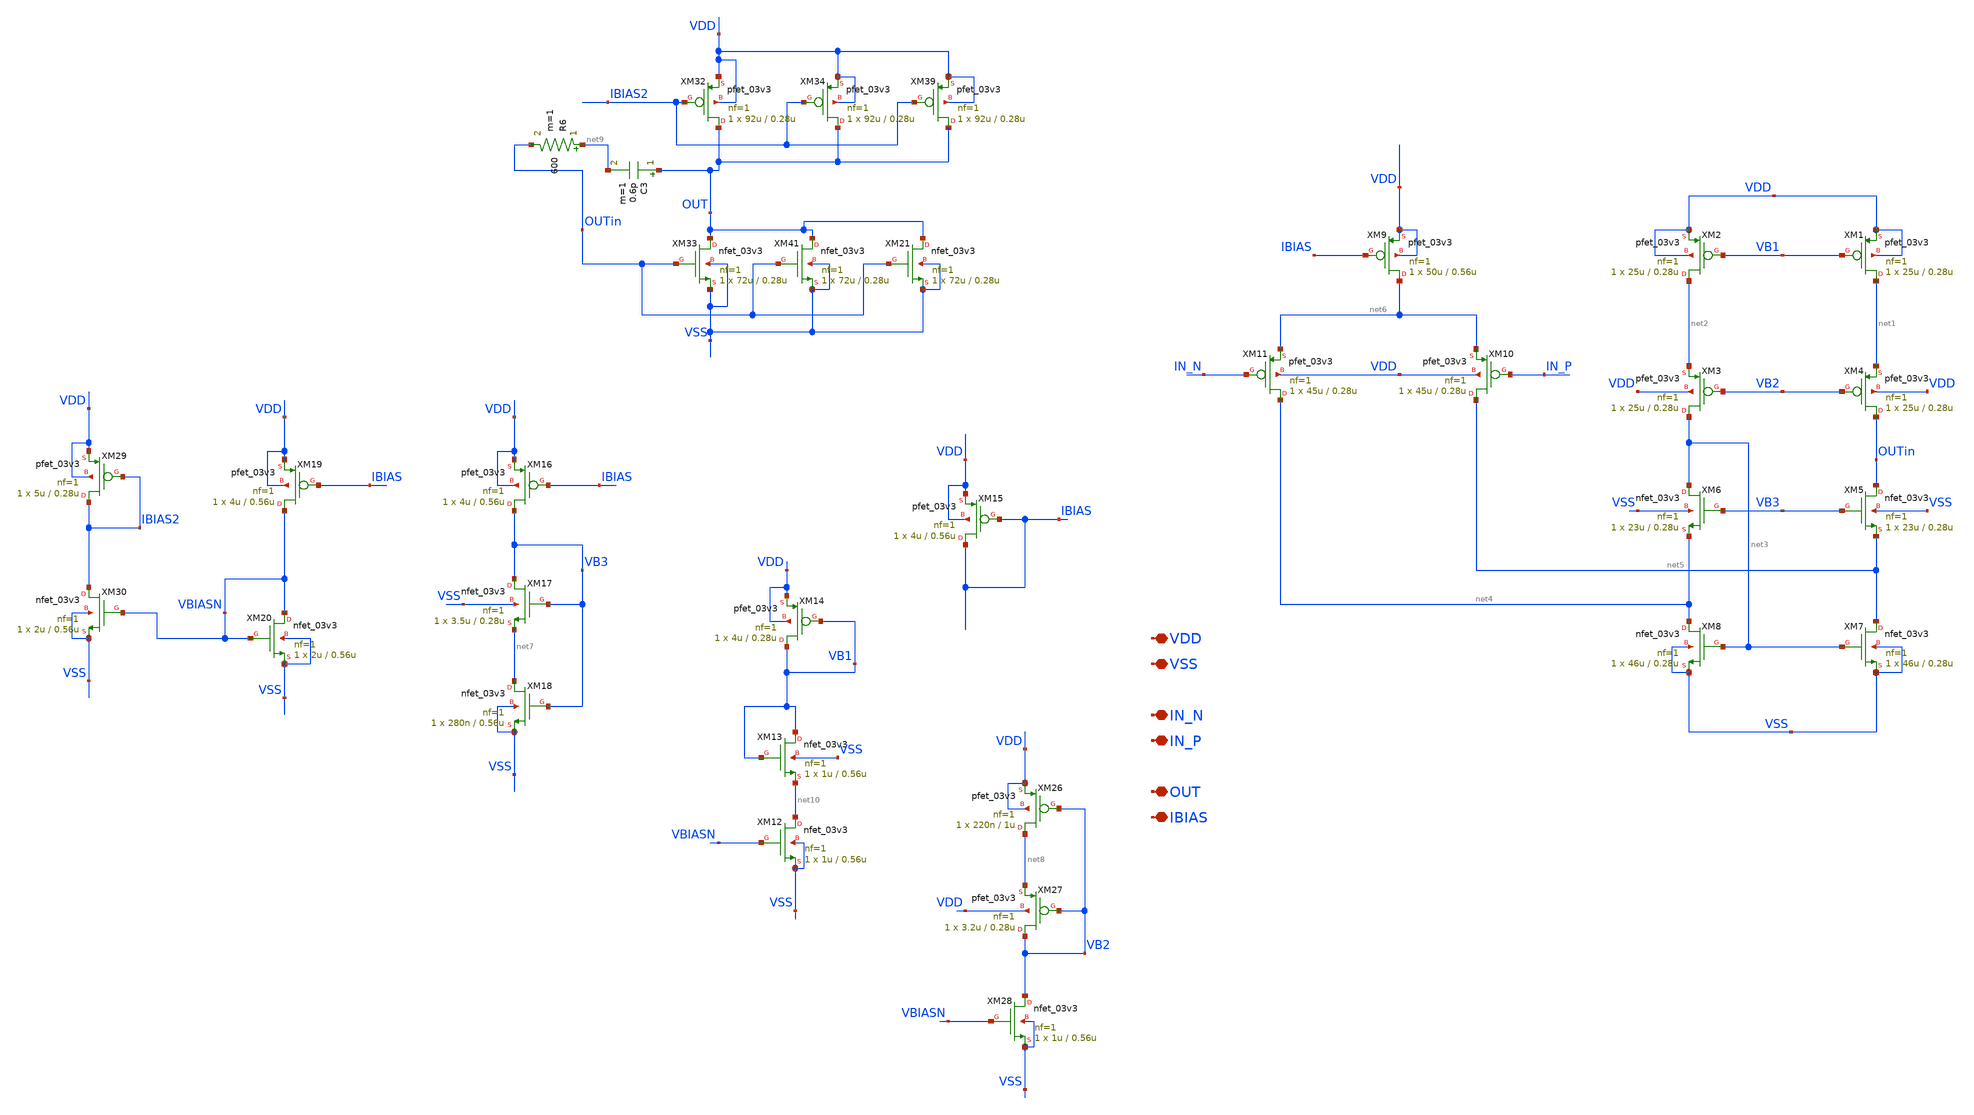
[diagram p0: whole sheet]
** sch_path: SCOP_INPUT_AND_MUX_PAKISTAN_03/Xschem/Folded_Cascode_Amplifier/Folded_opamp_single.sch
**.subckt Folded_opamp_single VDD VSS IN_N IN_P OUT IBIAS
*.iopin VDD
*.iopin VSS
*.iopin IN_N
*.iopin IN_P
*.iopin OUT
*.iopin IBIAS
XM1 net1 VB1 VDD VDD pfet_03v3 L=0.28u W=25u nf=1 ad='int((nf+1)/2) * W/nf * 0.18u' as='int((nf+2)/2) * W/nf * 0.18u'
+ pd='2*int((nf+1)/2) * (W/nf + 0.18u)' ps='2*int((nf+2)/2) * (W/nf + 0.18u)' nrd='0.18u / W' nrs='0.18u / W'
+ sa=0 sb=0 sd=0 m=1
XM2 net2 VB1 VDD VDD pfet_03v3 L=0.28u W=25u nf=1 ad='int((nf+1)/2) * W/nf * 0.18u' as='int((nf+2)/2) * W/nf * 0.18u'
+ pd='2*int((nf+1)/2) * (W/nf + 0.18u)' ps='2*int((nf+2)/2) * (W/nf + 0.18u)' nrd='0.18u / W' nrs='0.18u / W'
+ sa=0 sb=0 sd=0 m=1
XM3 net3 VB2 net2 VDD pfet_03v3 L=0.28u W=25u nf=1 ad='int((nf+1)/2) * W/nf * 0.18u' as='int((nf+2)/2) * W/nf * 0.18u'
+ pd='2*int((nf+1)/2) * (W/nf + 0.18u)' ps='2*int((nf+2)/2) * (W/nf + 0.18u)' nrd='0.18u / W' nrs='0.18u / W'
+ sa=0 sb=0 sd=0 m=1
XM4 OUTin VB2 net1 VDD pfet_03v3 L=0.28u W=25u nf=1 ad='int((nf+1)/2) * W/nf * 0.18u' as='int((nf+2)/2) * W/nf * 0.18u'
+ pd='2*int((nf+1)/2) * (W/nf + 0.18u)' ps='2*int((nf+2)/2) * (W/nf + 0.18u)' nrd='0.18u / W' nrs='0.18u / W'
+ sa=0 sb=0 sd=0 m=1
XM5 OUTin VB3 net5 VSS nfet_03v3 L=0.28u W=23u nf=1 ad='int((nf+1)/2) * W/nf * 0.18u' as='int((nf+2)/2) * W/nf * 0.18u'
+ pd='2*int((nf+1)/2) * (W/nf + 0.18u)' ps='2*int((nf+2)/2) * (W/nf + 0.18u)' nrd='0.18u / W' nrs='0.18u / W'
+ sa=0 sb=0 sd=0 m=1
XM6 net3 VB3 net4 VSS nfet_03v3 L=0.28u W=23u nf=1 ad='int((nf+1)/2) * W/nf * 0.18u' as='int((nf+2)/2) * W/nf * 0.18u'
+ pd='2*int((nf+1)/2) * (W/nf + 0.18u)' ps='2*int((nf+2)/2) * (W/nf + 0.18u)' nrd='0.18u / W' nrs='0.18u / W'
+ sa=0 sb=0 sd=0 m=1
XM7 net5 net3 VSS VSS nfet_03v3 L=0.28u W=46u nf=1 ad='int((nf+1)/2) * W/nf * 0.18u' as='int((nf+2)/2) * W/nf * 0.18u'
+ pd='2*int((nf+1)/2) * (W/nf + 0.18u)' ps='2*int((nf+2)/2) * (W/nf + 0.18u)' nrd='0.18u / W' nrs='0.18u / W'
+ sa=0 sb=0 sd=0 m=1
XM8 net4 net3 VSS VSS nfet_03v3 L=0.28u W=46u nf=1 ad='int((nf+1)/2) * W/nf * 0.18u' as='int((nf+2)/2) * W/nf * 0.18u'
+ pd='2*int((nf+1)/2) * (W/nf + 0.18u)' ps='2*int((nf+2)/2) * (W/nf + 0.18u)' nrd='0.18u / W' nrs='0.18u / W'
+ sa=0 sb=0 sd=0 m=1
XM9 net6 IBIAS VDD VDD pfet_03v3 L=0.56u W=50u nf=1 ad='int((nf+1)/2) * W/nf * 0.18u' as='int((nf+2)/2) * W/nf * 0.18u'
+ pd='2*int((nf+1)/2) * (W/nf + 0.18u)' ps='2*int((nf+2)/2) * (W/nf + 0.18u)' nrd='0.18u / W' nrs='0.18u / W'
+ sa=0 sb=0 sd=0 m=1
XM10 net5 IN_P net6 VDD pfet_03v3 L=0.28u W=45u nf=1 ad='int((nf+1)/2) * W/nf * 0.18u' as='int((nf+2)/2) * W/nf * 0.18u'
+ pd='2*int((nf+1)/2) * (W/nf + 0.18u)' ps='2*int((nf+2)/2) * (W/nf + 0.18u)' nrd='0.18u / W' nrs='0.18u / W'
+ sa=0 sb=0 sd=0 m=1
XM11 net4 IN_N net6 VDD pfet_03v3 L=0.28u W=45u nf=1 ad='int((nf+1)/2) * W/nf * 0.18u' as='int((nf+2)/2) * W/nf * 0.18u'
+ pd='2*int((nf+1)/2) * (W/nf + 0.18u)' ps='2*int((nf+2)/2) * (W/nf + 0.18u)' nrd='0.18u / W' nrs='0.18u / W'
+ sa=0 sb=0 sd=0 m=1
XM15 IBIAS IBIAS VDD VDD pfet_03v3 L=0.56u W=4u nf=1 ad='int((nf+1)/2) * W/nf * 0.18u' as='int((nf+2)/2) * W/nf * 0.18u'
+ pd='2*int((nf+1)/2) * (W/nf + 0.18u)' ps='2*int((nf+2)/2) * (W/nf + 0.18u)' nrd='0.18u / W' nrs='0.18u / W'
+ sa=0 sb=0 sd=0 m=1
XM16 VB3 IBIAS VDD VDD pfet_03v3 L=0.56u W=4u nf=1 ad='int((nf+1)/2) * W/nf * 0.18u' as='int((nf+2)/2) * W/nf * 0.18u'
+ pd='2*int((nf+1)/2) * (W/nf + 0.18u)' ps='2*int((nf+2)/2) * (W/nf + 0.18u)' nrd='0.18u / W' nrs='0.18u / W'
+ sa=0 sb=0 sd=0 m=1
XM17 VB3 VB3 net7 VSS nfet_03v3 L=0.28u W=3.5u nf=1 ad='int((nf+1)/2) * W/nf * 0.18u' as='int((nf+2)/2) * W/nf * 0.18u'
+ pd='2*int((nf+1)/2) * (W/nf + 0.18u)' ps='2*int((nf+2)/2) * (W/nf + 0.18u)' nrd='0.18u / W' nrs='0.18u / W'
+ sa=0 sb=0 sd=0 m=1
XM18 net7 VB3 VSS VSS nfet_03v3 L=0.56u W=280n nf=1 ad='int((nf+1)/2) * W/nf * 0.18u' as='int((nf+2)/2) * W/nf * 0.18u'
+ pd='2*int((nf+1)/2) * (W/nf + 0.18u)' ps='2*int((nf+2)/2) * (W/nf + 0.18u)' nrd='0.18u / W' nrs='0.18u / W'
+ sa=0 sb=0 sd=0 m=1
XM19 VBIASN IBIAS VDD VDD pfet_03v3 L=0.56u W=4u nf=1 ad='int((nf+1)/2) * W/nf * 0.18u' as='int((nf+2)/2) * W/nf * 0.18u'
+ pd='2*int((nf+1)/2) * (W/nf + 0.18u)' ps='2*int((nf+2)/2) * (W/nf + 0.18u)' nrd='0.18u / W' nrs='0.18u / W'
+ sa=0 sb=0 sd=0 m=1
XM20 VBIASN VBIASN VSS VSS nfet_03v3 L=0.56u W=2u nf=1 ad='int((nf+1)/2) * W/nf * 0.18u' as='int((nf+2)/2) * W/nf * 0.18u'
+ pd='2*int((nf+1)/2) * (W/nf + 0.18u)' ps='2*int((nf+2)/2) * (W/nf + 0.18u)' nrd='0.18u / W' nrs='0.18u / W'
+ sa=0 sb=0 sd=0 m=1
XM26 net8 VB2 VDD VDD pfet_03v3 L=1u W=220n nf=1 ad='int((nf+1)/2) * W/nf * 0.18u' as='int((nf+2)/2) * W/nf * 0.18u'
+ pd='2*int((nf+1)/2) * (W/nf + 0.18u)' ps='2*int((nf+2)/2) * (W/nf + 0.18u)' nrd='0.18u / W' nrs='0.18u / W'
+ sa=0 sb=0 sd=0 m=1
XM27 VB2 VB2 net8 VDD pfet_03v3 L=0.28u W=3.2u nf=1 ad='int((nf+1)/2) * W/nf * 0.18u' as='int((nf+2)/2) * W/nf * 0.18u'
+ pd='2*int((nf+1)/2) * (W/nf + 0.18u)' ps='2*int((nf+2)/2) * (W/nf + 0.18u)' nrd='0.18u / W' nrs='0.18u / W'
+ sa=0 sb=0 sd=0 m=1
XM28 VB2 VBIASN VSS VSS nfet_03v3 L=0.56u W=1u nf=1 ad='int((nf+1)/2) * W/nf * 0.18u' as='int((nf+2)/2) * W/nf * 0.18u'
+ pd='2*int((nf+1)/2) * (W/nf + 0.18u)' ps='2*int((nf+2)/2) * (W/nf + 0.18u)' nrd='0.18u / W' nrs='0.18u / W'
+ sa=0 sb=0 sd=0 m=1
XM29 IBIAS2 IBIAS2 VDD VDD pfet_03v3 L=0.28u W=5u nf=1 ad='int((nf+1)/2) * W/nf * 0.18u' as='int((nf+2)/2) * W/nf * 0.18u'
+ pd='2*int((nf+1)/2) * (W/nf + 0.18u)' ps='2*int((nf+2)/2) * (W/nf + 0.18u)' nrd='0.18u / W' nrs='0.18u / W'
+ sa=0 sb=0 sd=0 m=1
XM30 IBIAS2 VBIASN VSS VSS nfet_03v3 L=0.56u W=2u nf=1 ad='int((nf+1)/2) * W/nf * 0.18u' as='int((nf+2)/2) * W/nf * 0.18u'
+ pd='2*int((nf+1)/2) * (W/nf + 0.18u)' ps='2*int((nf+2)/2) * (W/nf + 0.18u)' nrd='0.18u / W' nrs='0.18u / W'
+ sa=0 sb=0 sd=0 m=1
XM32 OUT IBIAS2 VDD VDD pfet_03v3 L=0.28u W=92u nf=1 ad='int((nf+1)/2) * W/nf * 0.18u' as='int((nf+2)/2) * W/nf * 0.18u'
+ pd='2*int((nf+1)/2) * (W/nf + 0.18u)' ps='2*int((nf+2)/2) * (W/nf + 0.18u)' nrd='0.18u / W' nrs='0.18u / W'
+ sa=0 sb=0 sd=0 m=1
XM33 OUT OUTin VSS VSS nfet_03v3 L=0.28u W=72u nf=1 ad='int((nf+1)/2) * W/nf * 0.18u' as='int((nf+2)/2) * W/nf * 0.18u'
+ pd='2*int((nf+1)/2) * (W/nf + 0.18u)' ps='2*int((nf+2)/2) * (W/nf + 0.18u)' nrd='0.18u / W' nrs='0.18u / W'
+ sa=0 sb=0 sd=0 m=1
C3 OUT net9 0.6p m=1
XM34 OUT IBIAS2 VDD VDD pfet_03v3 L=0.28u W=92u nf=1 ad='int((nf+1)/2) * W/nf * 0.18u' as='int((nf+2)/2) * W/nf * 0.18u'
+ pd='2*int((nf+1)/2) * (W/nf + 0.18u)' ps='2*int((nf+2)/2) * (W/nf + 0.18u)' nrd='0.18u / W' nrs='0.18u / W'
+ sa=0 sb=0 sd=0 m=1
R6 net9 OUTin 600 m=1
XM41 OUT OUTin VSS VSS nfet_03v3 L=0.28u W=72u nf=1 ad='int((nf+1)/2) * W/nf * 0.18u' as='int((nf+2)/2) * W/nf * 0.18u'
+ pd='2*int((nf+1)/2) * (W/nf + 0.18u)' ps='2*int((nf+2)/2) * (W/nf + 0.18u)' nrd='0.18u / W' nrs='0.18u / W'
+ sa=0 sb=0 sd=0 m=1
XM39 OUT IBIAS2 VDD VDD pfet_03v3 L=0.28u W=92u nf=1 ad='int((nf+1)/2) * W/nf * 0.18u' as='int((nf+2)/2) * W/nf * 0.18u'
+ pd='2*int((nf+1)/2) * (W/nf + 0.18u)' ps='2*int((nf+2)/2) * (W/nf + 0.18u)' nrd='0.18u / W' nrs='0.18u / W'
+ sa=0 sb=0 sd=0 m=1
XM12 net10 VBIASN VSS VSS nfet_03v3 L=0.56u W=1u nf=1 ad='int((nf+1)/2) * W/nf * 0.18u' as='int((nf+2)/2) * W/nf * 0.18u'
+ pd='2*int((nf+1)/2) * (W/nf + 0.18u)' ps='2*int((nf+2)/2) * (W/nf + 0.18u)' nrd='0.18u / W' nrs='0.18u / W'
+ sa=0 sb=0 sd=0 m=1
XM13 VB1 VB1 net10 VSS nfet_03v3 L=0.56u W=1u nf=1 ad='int((nf+1)/2) * W/nf * 0.18u' as='int((nf+2)/2) * W/nf * 0.18u'
+ pd='2*int((nf+1)/2) * (W/nf + 0.18u)' ps='2*int((nf+2)/2) * (W/nf + 0.18u)' nrd='0.18u / W' nrs='0.18u / W'
+ sa=0 sb=0 sd=0 m=1
XM14 VB1 VB1 VDD VDD pfet_03v3 L=0.28u W=4u nf=1 ad='int((nf+1)/2) * W/nf * 0.18u' as='int((nf+2)/2) * W/nf * 0.18u'
+ pd='2*int((nf+1)/2) * (W/nf + 0.18u)' ps='2*int((nf+2)/2) * (W/nf + 0.18u)' nrd='0.18u / W' nrs='0.18u / W'
+ sa=0 sb=0 sd=0 m=1
XM21 OUT OUTin VSS VSS nfet_03v3 L=0.28u W=72u nf=1 ad='int((nf+1)/2) * W/nf * 0.18u' as='int((nf+2)/2) * W/nf * 0.18u'
+ pd='2*int((nf+1)/2) * (W/nf + 0.18u)' ps='2*int((nf+2)/2) * (W/nf + 0.18u)' nrd='0.18u / W' nrs='0.18u / W'
+ sa=0 sb=0 sd=0 m=1
**.ends
.end
